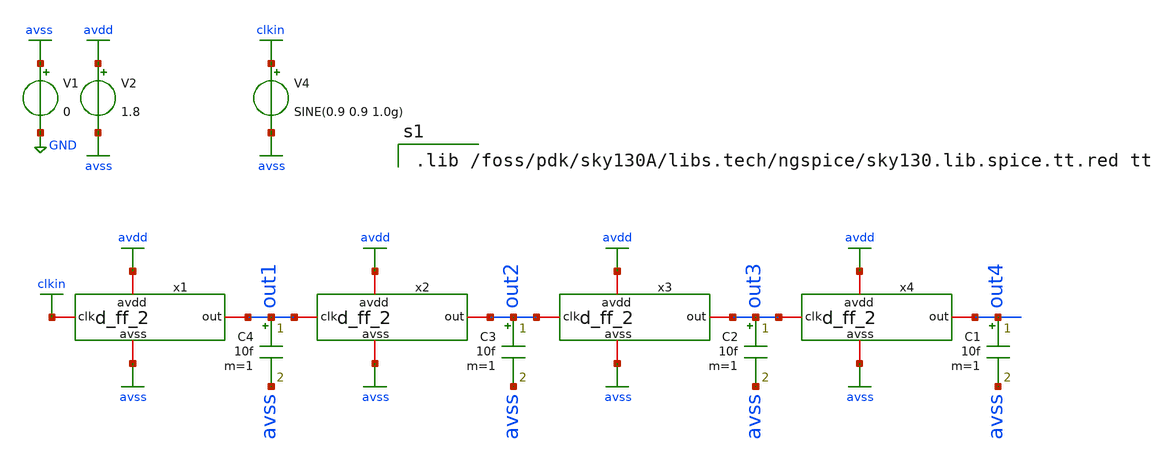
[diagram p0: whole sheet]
** sch_path: xschem/d_ff_sim5.sch
**.subckt d_ff_sim5
V1 avss GND 0
V2 avdd avss 1.8
V4 clkin avss SINE(0.9 0.9 1.0g)
C1 out4 avss 10f m=1
x1 avdd avss clkin out1 d_ff_2
x2 avdd avss out1 out2 d_ff_2
x3 avdd avss out2 out3 d_ff_2
x4 avdd avss out3 out4 d_ff_2
C2 out3 avss 10f m=1
C3 out2 avss 10f m=1
C4 out1 avss 10f m=1
**** begin user architecture code

.lib /foss/pdk/sky130A/libs.tech/ngspice/sky130.lib.spice.tt.red tt



.control
set temp=25
save clkin out1 out2 out3 out4 @V1[i]
tran 0.01n 500n 20n
*plot @V1[i]
plot clkin out4
fft clkin out1 out2 out3 out4
*plot db(mag(out1)) xlimit 0.1g 15g ylimit 0.0 -200
*plot db(mag(clkin)) xlimit 0.1g 15g ylimit 0.0 -200
plot db(mag(clkin)) db(mag(out1)) db(mag(out2)) db(mag(out3)) db(mag(out4)) xlimit 0.1g 10g ylimit
+ 0.0 -200
.endc
.end


**** end user architecture code
**.ends

* expanding   symbol:  ma2022/d_ff_2.sym # of pins=4
** sym_path: xschem/d_ff_2.sym
** sch_path: xschem/d_ff_2.sch
.subckt d_ff_2 avdd avss clk out
*.iopin avdd
*.iopin avss
*.iopin clk
*.iopin out
XM4 net7 clk net1 avdd sky130_fd_pr__pfet_01v8 L=0.15 W=8.4 nf=1 ad='int((nf+1)/2) * W/nf * 0.29' as='int((nf+2)/2) * W/nf * 0.29'
+ pd='2*int((nf+1)/2) * (W/nf + 0.29)' ps='2*int((nf+2)/2) * (W/nf + 0.29)' nrd='0.29 / W' nrs='0.29 / W'
+ sa=0 sb=0 sd=0 mult=1 m=1
XM1 net1 s2 avdd avdd sky130_fd_pr__pfet_01v8 L=0.15 W=8.4 nf=1 ad='int((nf+1)/2) * W/nf * 0.29' as='int((nf+2)/2) * W/nf * 0.29'
+ pd='2*int((nf+1)/2) * (W/nf + 0.29)' ps='2*int((nf+2)/2) * (W/nf + 0.29)' nrd='0.29 / W' nrs='0.29 / W'
+ sa=0 sb=0 sd=0 mult=1 m=1
XM11 net7 s2 avss avss sky130_fd_pr__nfet_01v8 L=0.15 W=4.2 nf=5 ad='int((nf+1)/2) * W/nf * 0.29' as='int((nf+2)/2) * W/nf * 0.29'
+ pd='2*int((nf+1)/2) * (W/nf + 0.29)' ps='2*int((nf+2)/2) * (W/nf + 0.29)' nrd='0.29 / W' nrs='0.29 / W'
+ sa=0 sb=0 sd=0 mult=1 m=1
XM3 net2 clk net4 avss sky130_fd_pr__nfet_01v8 L=0.15 W=2.8 nf=4 ad='int((nf+1)/2) * W/nf * 0.29' as='int((nf+2)/2) * W/nf * 0.29'
+ pd='2*int((nf+1)/2) * (W/nf + 0.29)' ps='2*int((nf+2)/2) * (W/nf + 0.29)' nrd='0.29 / W' nrs='0.29 / W'
+ sa=0 sb=0 sd=0 mult=1 m=1
XM5 net2 clk net3 avdd sky130_fd_pr__pfet_01v8 L=0.15 W=7.0 nf=5 ad='int((nf+1)/2) * W/nf * 0.29' as='int((nf+2)/2) * W/nf * 0.29'
+ pd='2*int((nf+1)/2) * (W/nf + 0.29)' ps='2*int((nf+2)/2) * (W/nf + 0.29)' nrd='0.29 / W' nrs='0.29 / W'
+ sa=0 sb=0 sd=0 mult=1 m=1
XM2 net3 net7 avdd avdd sky130_fd_pr__pfet_01v8 L=0.15 W=7.0 nf=5 ad='int((nf+1)/2) * W/nf * 0.29' as='int((nf+2)/2) * W/nf * 0.29'
+ pd='2*int((nf+1)/2) * (W/nf + 0.29)' ps='2*int((nf+2)/2) * (W/nf + 0.29)' nrd='0.29 / W' nrs='0.29 / W'
+ sa=0 sb=0 sd=0 mult=1 m=1
XM6 net4 net7 avss avss sky130_fd_pr__nfet_01v8 L=0.15 W=2.8 nf=4 ad='int((nf+1)/2) * W/nf * 0.29' as='int((nf+2)/2) * W/nf * 0.29'
+ pd='2*int((nf+1)/2) * (W/nf + 0.29)' ps='2*int((nf+2)/2) * (W/nf + 0.29)' nrd='0.29 / W' nrs='0.29 / W'
+ sa=0 sb=0 sd=0 mult=1 m=1
XM8 s2 clk net5 avss sky130_fd_pr__nfet_01v8 L=0.15 W=2.8 nf=3 ad='int((nf+1)/2) * W/nf * 0.29' as='int((nf+2)/2) * W/nf * 0.29'
+ pd='2*int((nf+1)/2) * (W/nf + 0.29)' ps='2*int((nf+2)/2) * (W/nf + 0.29)' nrd='0.29 / W' nrs='0.29 / W'
+ sa=0 sb=0 sd=0 mult=1 m=1
XM15 s2 net2 avdd avdd sky130_fd_pr__pfet_01v8 L=0.15 W=5.6 nf=6 ad='int((nf+1)/2) * W/nf * 0.29' as='int((nf+2)/2) * W/nf * 0.29'
+ pd='2*int((nf+1)/2) * (W/nf + 0.29)' ps='2*int((nf+2)/2) * (W/nf + 0.29)' nrd='0.29 / W' nrs='0.29 / W'
+ sa=0 sb=0 sd=0 mult=1 m=1
XM7 net5 net2 avss avss sky130_fd_pr__nfet_01v8 L=0.15 W=2.8 nf=3 ad='int((nf+1)/2) * W/nf * 0.29' as='int((nf+2)/2) * W/nf * 0.29'
+ pd='2*int((nf+1)/2) * (W/nf + 0.29)' ps='2*int((nf+2)/2) * (W/nf + 0.29)' nrd='0.29 / W' nrs='0.29 / W'
+ sa=0 sb=0 sd=0 mult=1 m=1
XM19 net6 s2 avdd avdd sky130_fd_pr__pfet_01v8 L=0.15 W=2.8 nf=5 ad='int((nf+1)/2) * W/nf * 0.29' as='int((nf+2)/2) * W/nf * 0.29'
+ pd='2*int((nf+1)/2) * (W/nf + 0.29)' ps='2*int((nf+2)/2) * (W/nf + 0.29)' nrd='0.29 / W' nrs='0.29 / W'
+ sa=0 sb=0 sd=0 mult=1 m=1
XM20 net6 s2 avss avss sky130_fd_pr__nfet_01v8 L=0.15 W=1.4 nf=1 ad='int((nf+1)/2) * W/nf * 0.29' as='int((nf+2)/2) * W/nf * 0.29'
+ pd='2*int((nf+1)/2) * (W/nf + 0.29)' ps='2*int((nf+2)/2) * (W/nf + 0.29)' nrd='0.29 / W' nrs='0.29 / W'
+ sa=0 sb=0 sd=0 mult=1 m=1
XM9 out net6 avdd avdd sky130_fd_pr__pfet_01v8 L=0.15 W=5.6 nf=5 ad='int((nf+1)/2) * W/nf * 0.29' as='int((nf+2)/2) * W/nf * 0.29'
+ pd='2*int((nf+1)/2) * (W/nf + 0.29)' ps='2*int((nf+2)/2) * (W/nf + 0.29)' nrd='0.29 / W' nrs='0.29 / W'
+ sa=0 sb=0 sd=0 mult=1 m=1
XM10 out net6 avss avss sky130_fd_pr__nfet_01v8 L=0.15 W=2.8 nf=1 ad='int((nf+1)/2) * W/nf * 0.29' as='int((nf+2)/2) * W/nf * 0.29'
+ pd='2*int((nf+1)/2) * (W/nf + 0.29)' ps='2*int((nf+2)/2) * (W/nf + 0.29)' nrd='0.29 / W' nrs='0.29 / W'
+ sa=0 sb=0 sd=0 mult=1 m=1
.ends

.GLOBAL avdd
.GLOBAL avss
.GLOBAL GND
.GLOBAL clkin
.end
